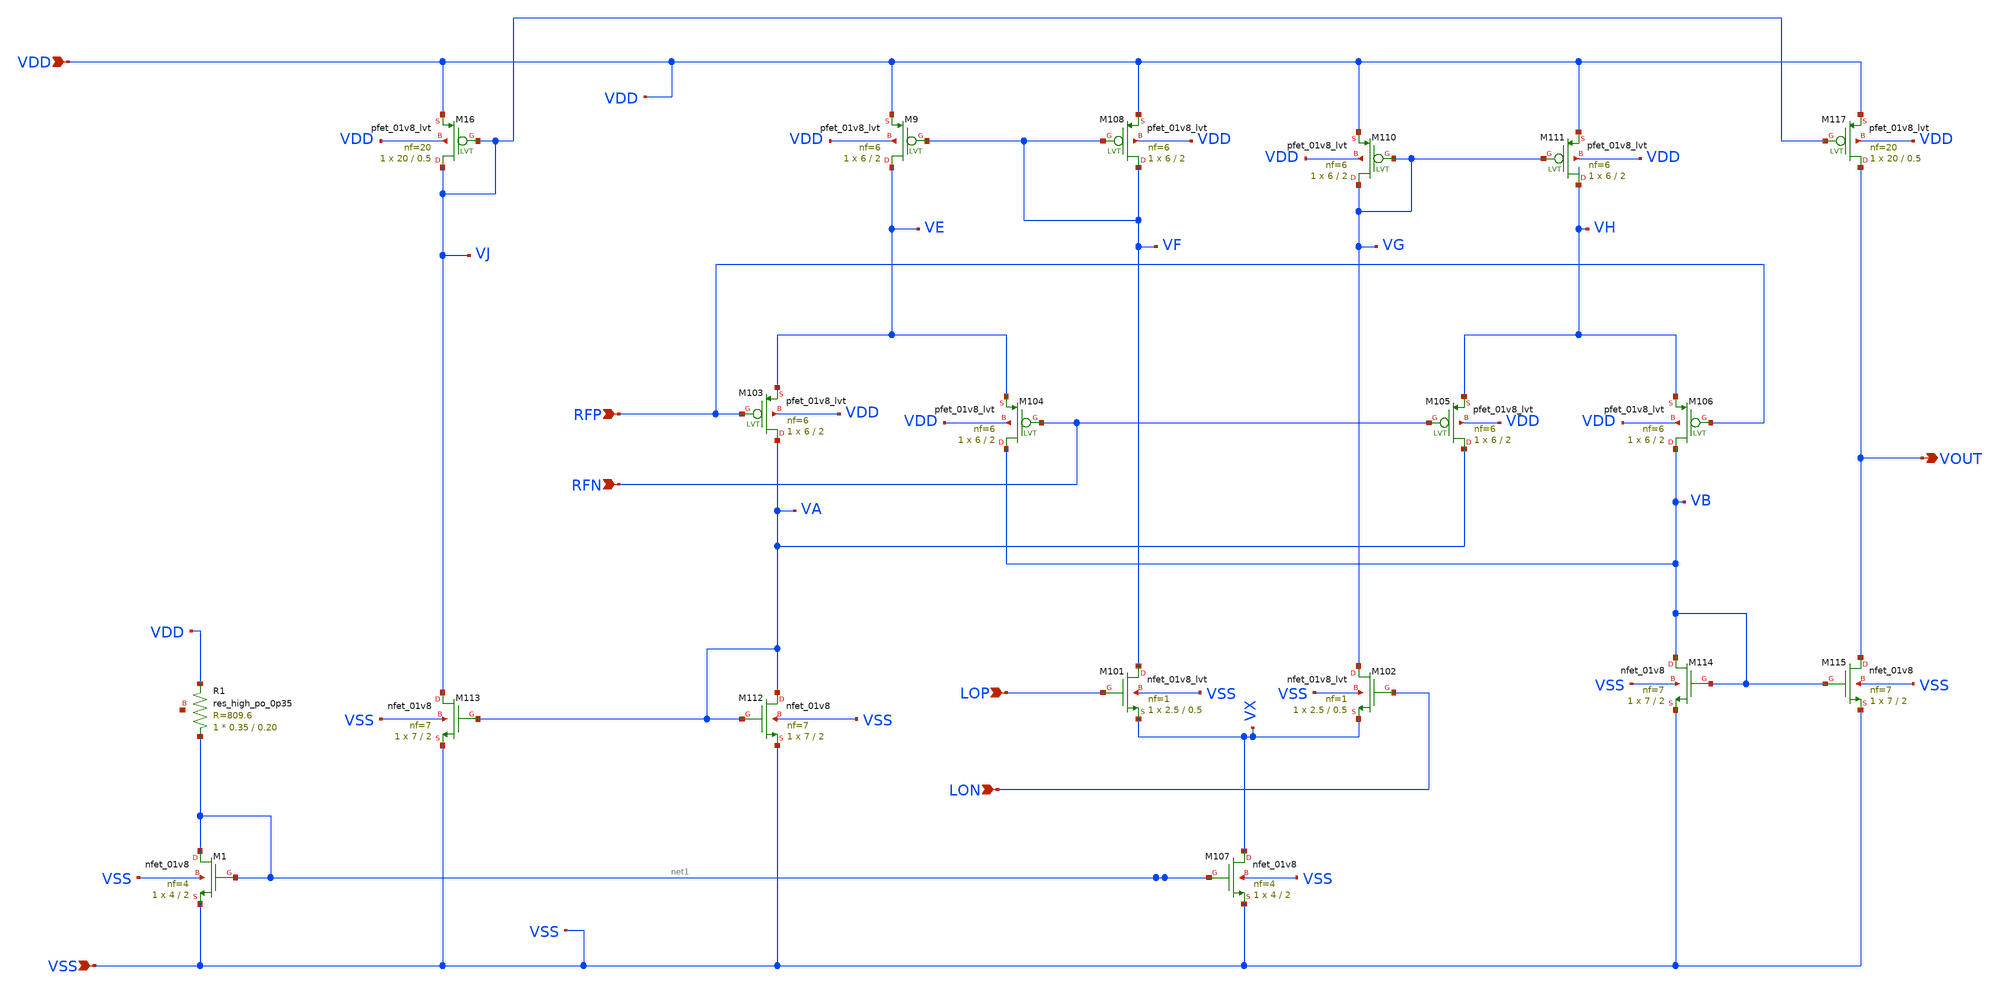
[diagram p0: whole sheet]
** sch_path: xschem/multiplier.sch
**.subckt multiplier LOP RFP LON VSS RFN VDD VOUT
*.ipin LOP
*.ipin RFP
*.ipin LON
*.ipin VSS
*.ipin RFN
*.ipin VDD
*.opin VOUT
XM107 VX net1 VSS VSS sky130_fd_pr__nfet_01v8 L=2 W=4 nf=4 ad='int((nf+1)/2) * W/nf * 0.29' as='int((nf+2)/2) * W/nf * 0.29'
+ pd='2*int((nf+1)/2) * (W/nf + 0.29)' ps='2*int((nf+2)/2) * (W/nf + 0.29)' nrd='0.29 / W' nrs='0.29 / W'
+ sa=0 sb=0 sd=0 mult=1 m=1
XM115 VOUT VB VSS VSS sky130_fd_pr__nfet_01v8 L=2 W=7 nf=7 ad='int((nf+1)/2) * W/nf * 0.29' as='int((nf+2)/2) * W/nf * 0.29'
+ pd='2*int((nf+1)/2) * (W/nf + 0.29)' ps='2*int((nf+2)/2) * (W/nf + 0.29)' nrd='0.29 / W' nrs='0.29 / W'
+ sa=0 sb=0 sd=0 mult=1 m=1
XM101 VF LOP VX VSS sky130_fd_pr__nfet_01v8_lvt L=0.5 W=2.5 nf=1 ad='int((nf+1)/2) * W/nf * 0.29' as='int((nf+2)/2) * W/nf * 0.29'
+ pd='2*int((nf+1)/2) * (W/nf + 0.29)' ps='2*int((nf+2)/2) * (W/nf + 0.29)' nrd='0.29 / W' nrs='0.29 / W'
+ sa=0 sb=0 sd=0 mult=1 m=1
XM102 VG LON VX VSS sky130_fd_pr__nfet_01v8_lvt L=0.5 W=2.5 nf=1 ad='int((nf+1)/2) * W/nf * 0.29' as='int((nf+2)/2) * W/nf * 0.29'
+ pd='2*int((nf+1)/2) * (W/nf + 0.29)' ps='2*int((nf+2)/2) * (W/nf + 0.29)' nrd='0.29 / W' nrs='0.29 / W'
+ sa=0 sb=0 sd=0 mult=1 m=1
XM117 VOUT VJ VDD VDD sky130_fd_pr__pfet_01v8_lvt L=0.5 W=20 nf=20 ad='int((nf+1)/2) * W/nf * 0.29' as='int((nf+2)/2) * W/nf * 0.29'
+ pd='2*int((nf+1)/2) * (W/nf + 0.29)' ps='2*int((nf+2)/2) * (W/nf + 0.29)' nrd='0.29 / W' nrs='0.29 / W'
+ sa=0 sb=0 sd=0 mult=1 m=1
XM9 VE VF VDD VDD sky130_fd_pr__pfet_01v8_lvt L=2 W=6 nf=6 ad='int((nf+1)/2) * W/nf * 0.29' as='int((nf+2)/2) * W/nf * 0.29'
+ pd='2*int((nf+1)/2) * (W/nf + 0.29)' ps='2*int((nf+2)/2) * (W/nf + 0.29)' nrd='0.29 / W' nrs='0.29 / W'
+ sa=0 sb=0 sd=0 mult=1 m=1
XM110 VG VG VDD VDD sky130_fd_pr__pfet_01v8_lvt L=2 W=6 nf=6 ad='int((nf+1)/2) * W/nf * 0.29' as='int((nf+2)/2) * W/nf * 0.29'
+ pd='2*int((nf+1)/2) * (W/nf + 0.29)' ps='2*int((nf+2)/2) * (W/nf + 0.29)' nrd='0.29 / W' nrs='0.29 / W'
+ sa=0 sb=0 sd=0 mult=1 m=1
XM111 VH VG VDD VDD sky130_fd_pr__pfet_01v8_lvt L=2 W=6 nf=6 ad='int((nf+1)/2) * W/nf * 0.29' as='int((nf+2)/2) * W/nf * 0.29'
+ pd='2*int((nf+1)/2) * (W/nf + 0.29)' ps='2*int((nf+2)/2) * (W/nf + 0.29)' nrd='0.29 / W' nrs='0.29 / W'
+ sa=0 sb=0 sd=0 mult=1 m=1
XM108 VF VF VDD VDD sky130_fd_pr__pfet_01v8_lvt L=2 W=6 nf=6 ad='int((nf+1)/2) * W/nf * 0.29' as='int((nf+2)/2) * W/nf * 0.29'
+ pd='2*int((nf+1)/2) * (W/nf + 0.29)' ps='2*int((nf+2)/2) * (W/nf + 0.29)' nrd='0.29 / W' nrs='0.29 / W'
+ sa=0 sb=0 sd=0 mult=1 m=1
XM16 VJ VJ VDD VDD sky130_fd_pr__pfet_01v8_lvt L=0.5 W=20 nf=20 ad='int((nf+1)/2) * W/nf * 0.29' as='int((nf+2)/2) * W/nf * 0.29'
+ pd='2*int((nf+1)/2) * (W/nf + 0.29)' ps='2*int((nf+2)/2) * (W/nf + 0.29)' nrd='0.29 / W' nrs='0.29 / W'
+ sa=0 sb=0 sd=0 mult=1 m=1
XM105 VA RFN VH VDD sky130_fd_pr__pfet_01v8_lvt L=2 W=6 nf=6 ad='int((nf+1)/2) * W/nf * 0.29' as='int((nf+2)/2) * W/nf * 0.29'
+ pd='2*int((nf+1)/2) * (W/nf + 0.29)' ps='2*int((nf+2)/2) * (W/nf + 0.29)' nrd='0.29 / W' nrs='0.29 / W'
+ sa=0 sb=0 sd=0 mult=1 m=1
XM106 VB RFP VH VDD sky130_fd_pr__pfet_01v8_lvt L=2 W=6 nf=6 ad='int((nf+1)/2) * W/nf * 0.29' as='int((nf+2)/2) * W/nf * 0.29'
+ pd='2*int((nf+1)/2) * (W/nf + 0.29)' ps='2*int((nf+2)/2) * (W/nf + 0.29)' nrd='0.29 / W' nrs='0.29 / W'
+ sa=0 sb=0 sd=0 mult=1 m=1
XM103 VA RFP VE VDD sky130_fd_pr__pfet_01v8_lvt L=2 W=6 nf=6 ad='int((nf+1)/2) * W/nf * 0.29' as='int((nf+2)/2) * W/nf * 0.29'
+ pd='2*int((nf+1)/2) * (W/nf + 0.29)' ps='2*int((nf+2)/2) * (W/nf + 0.29)' nrd='0.29 / W' nrs='0.29 / W'
+ sa=0 sb=0 sd=0 mult=1 m=1
XM104 VB RFN VE VDD sky130_fd_pr__pfet_01v8_lvt L=2 W=6 nf=6 ad='int((nf+1)/2) * W/nf * 0.29' as='int((nf+2)/2) * W/nf * 0.29'
+ pd='2*int((nf+1)/2) * (W/nf + 0.29)' ps='2*int((nf+2)/2) * (W/nf + 0.29)' nrd='0.29 / W' nrs='0.29 / W'
+ sa=0 sb=0 sd=0 mult=1 m=1
XM114 VB VB VSS VSS sky130_fd_pr__nfet_01v8 L=2 W=7 nf=7 ad='int((nf+1)/2) * W/nf * 0.29' as='int((nf+2)/2) * W/nf * 0.29'
+ pd='2*int((nf+1)/2) * (W/nf + 0.29)' ps='2*int((nf+2)/2) * (W/nf + 0.29)' nrd='0.29 / W' nrs='0.29 / W'
+ sa=0 sb=0 sd=0 mult=1 m=1
XM113 VJ VA VSS VSS sky130_fd_pr__nfet_01v8 L=2 W=7 nf=7 ad='int((nf+1)/2) * W/nf * 0.29' as='int((nf+2)/2) * W/nf * 0.29'
+ pd='2*int((nf+1)/2) * (W/nf + 0.29)' ps='2*int((nf+2)/2) * (W/nf + 0.29)' nrd='0.29 / W' nrs='0.29 / W'
+ sa=0 sb=0 sd=0 mult=1 m=1
XM112 VA VA VSS VSS sky130_fd_pr__nfet_01v8 L=2 W=7 nf=7 ad='int((nf+1)/2) * W/nf * 0.29' as='int((nf+2)/2) * W/nf * 0.29'
+ pd='2*int((nf+1)/2) * (W/nf + 0.29)' ps='2*int((nf+2)/2) * (W/nf + 0.29)' nrd='0.29 / W' nrs='0.29 / W'
+ sa=0 sb=0 sd=0 mult=1 m=1
XM1 net1 net1 VSS VSS sky130_fd_pr__nfet_01v8 L=2 W=4 nf=4 ad='int((nf+1)/2) * W/nf * 0.29' as='int((nf+2)/2) * W/nf * 0.29'
+ pd='2*int((nf+1)/2) * (W/nf + 0.29)' ps='2*int((nf+2)/2) * (W/nf + 0.29)' nrd='0.29 / W' nrs='0.29 / W'
+ sa=0 sb=0 sd=0 mult=1 m=1
XR1 net1 VDD net2 sky130_fd_pr__res_high_po_0p35 L=0.20 mult=1 m=1
**.ends
.end
